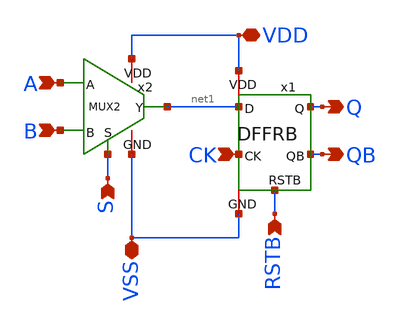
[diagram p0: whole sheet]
** sch_path: LEF/MUXDFFRB.sch
**.subckt MUXDFFRB A B CK Q QB VDD VSS S RSTB
*.ipin A
*.ipin B
*.ipin CK
*.opin Q
*.opin QB
*.iopin VDD
*.iopin VSS
*.ipin S
*.ipin RSTB
x1 VDD QB net1 Q RSTB VSS CK DFFRB
x2 A B S VDD net1 VSS MUX2
**.ends
.end
